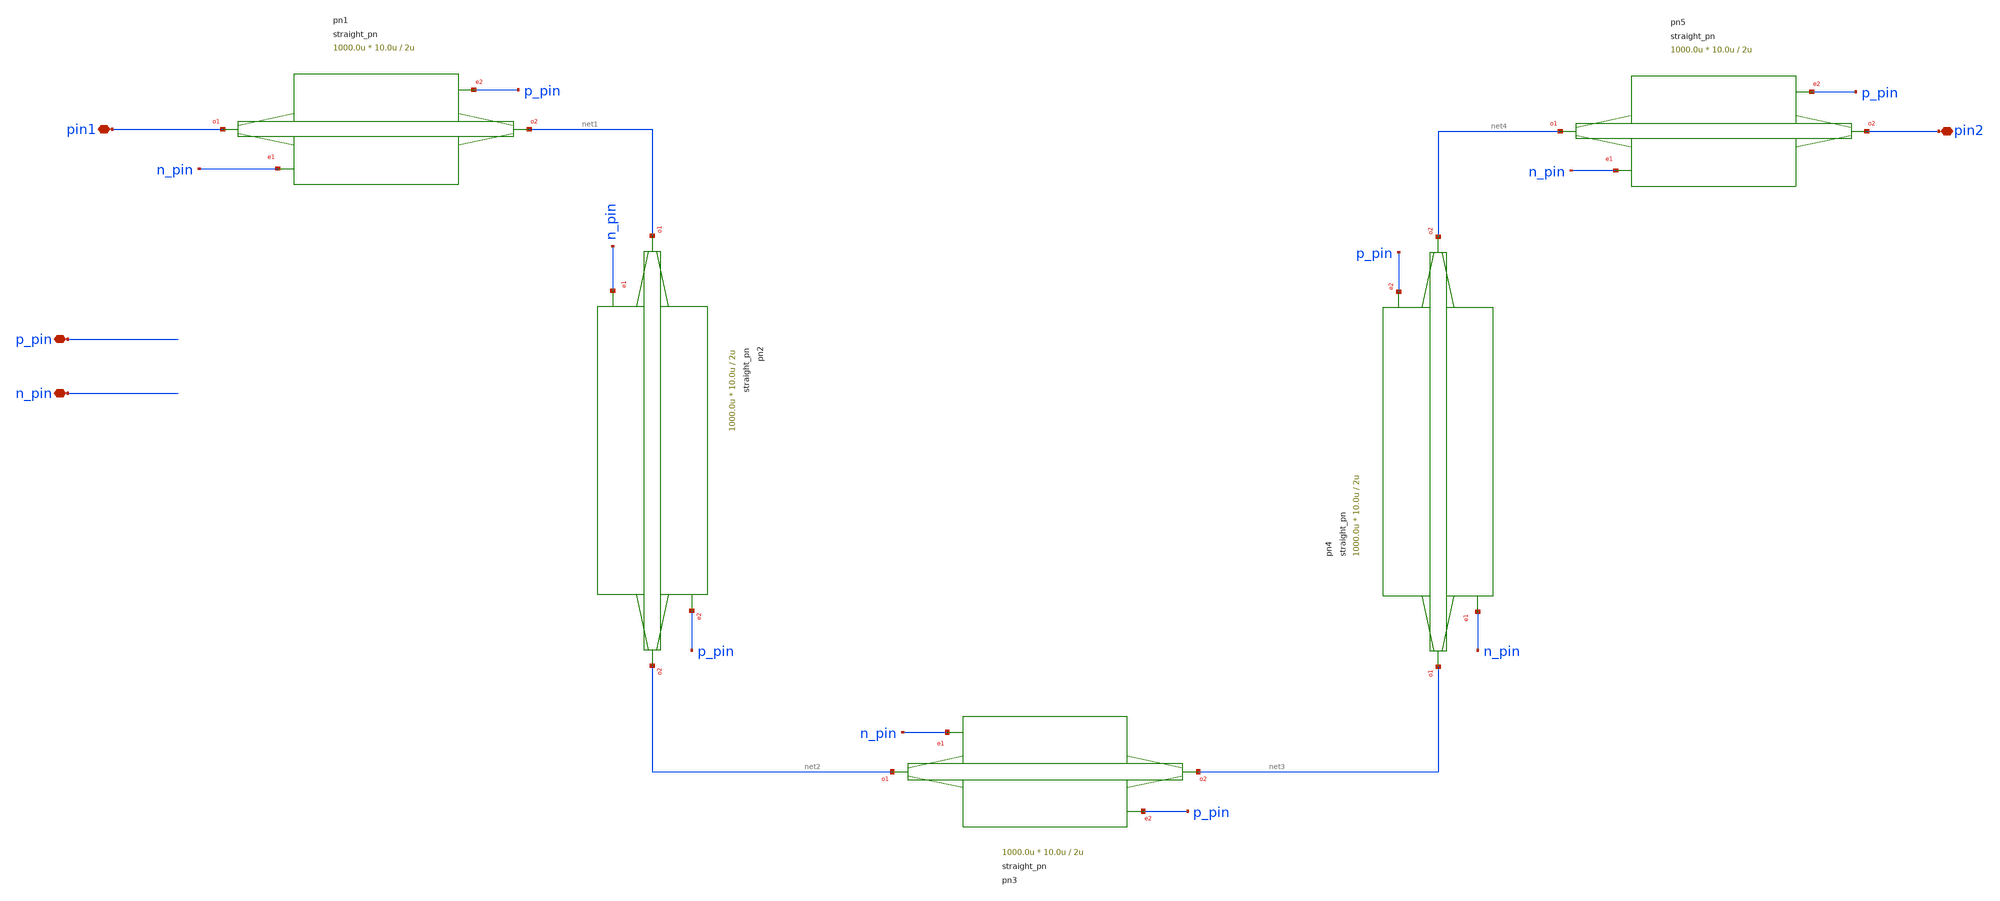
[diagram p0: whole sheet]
** sch_path: xschem/tests/test_sch/test_straight_pn.sch
* Copyright (c) 2024, Mabrains LLC
* Licensed under the GNU Lesser General Public License, Version 3.0 (the "License");
* you may not use this file except in compliance with the License.
* GNU Lesser General Public License
* Version 3, 29 June 2007
* This program is free software: you can redistribute it and/or modify
* it under the terms of the GNU Lesser General Public License as published
* by the Free Software Foundation, either version 3 of the License, or
* (at your option) any later version.
* This program is distributed in the hope that it will be useful,
* but WITHOUT ANY WARRANTY; without even the implied warranty of
* MERCHANTABILITY or FITNESS FOR A PARTICULAR PURPOSE.  See the
* GNU Lesser General Public License for more details.
* You should have received a copy of the GNU Lesser General Public License
* along with this program.  If not, see <https://www.gnu.org/licenses/>.
* SPDX-License-Identifier: LGPL-3.0
**.subckt test_straight_pn pin1 pin2 p_pin n_pin
*.iopin pin1
*.iopin pin2
*.iopin p_pin
*.iopin n_pin
Ppn1 pin1 net1 n_pin p_pin straight_pn length=1000.0u via_stack_width=10.0u via_stack_spacing=2u
Ppn2 net1 net2 n_pin p_pin straight_pn length=1000.0u via_stack_width=10.0u via_stack_spacing=2u
Ppn3 net2 net3 n_pin p_pin straight_pn length=1000.0u via_stack_width=10.0u via_stack_spacing=2u
Ppn4 net3 net4 n_pin p_pin straight_pn length=1000.0u via_stack_width=10.0u via_stack_spacing=2u
Ppn5 net4 pin2 n_pin p_pin straight_pn length=1000.0u via_stack_width=10.0u via_stack_spacing=2u
**.ends
.end
